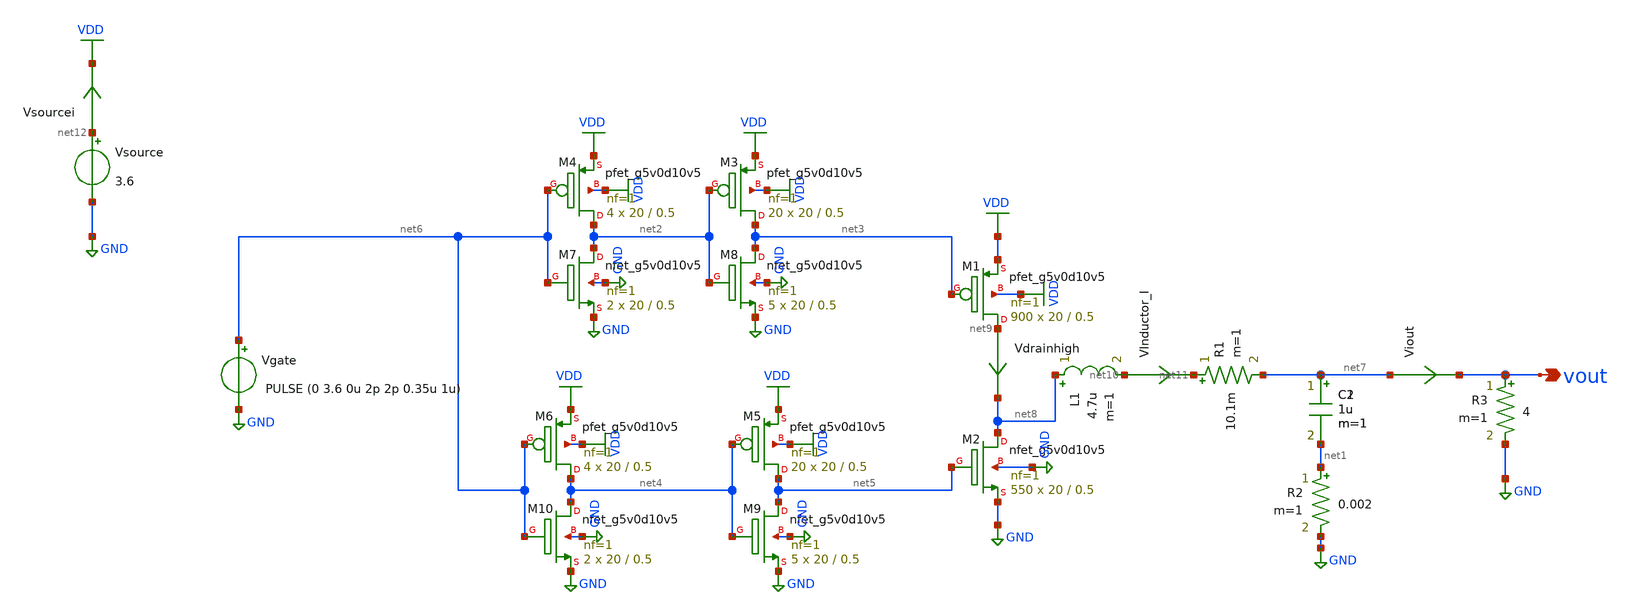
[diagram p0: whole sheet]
** sch_path: SMPS_Without_Deadtime/buck_converter.sch
**.subckt buck_converter vout
*.opin vout
XM1 net9 net3 VDD VDD sky130_fd_pr__pfet_g5v0d10v5 L=0.5 W=20 nf=1 ad='int((nf+1)/2) * W/nf * 0.29' as='int((nf+2)/2) * W/nf * 0.29'
+ pd='2*int((nf+1)/2) * (W/nf + 0.29)' ps='2*int((nf+2)/2) * (W/nf + 0.29)' nrd='0.29 / W' nrs='0.29 / W'
+ sa=0 sb=0 sd=0 mult=900 m=900
XM2 net8 net5 GND GND sky130_fd_pr__nfet_g5v0d10v5 L=0.5 W=20 nf=1 ad='int((nf+1)/2) * W/nf * 0.29' as='int((nf+2)/2) * W/nf * 0.29'
+ pd='2*int((nf+1)/2) * (W/nf + 0.29)' ps='2*int((nf+2)/2) * (W/nf + 0.29)' nrd='0.29 / W' nrs='0.29 / W'
+ sa=0 sb=0 sd=0 mult=550 m=550
L1 net8 net10 4.7u m=1
R1 net11 net7 10.1m m=1
C1 net7 net1 1u m=1
R2 net1 GND 0.002 m=1
Vgate net6 GND PULSE (0 3.6 0u 2p 2p 0.35u 1u)
Vsource net12 GND 3.6
XM3 net3 net2 VDD VDD sky130_fd_pr__pfet_g5v0d10v5 L=0.5 W=20 nf=1 ad='int((nf+1)/2) * W/nf * 0.29' as='int((nf+2)/2) * W/nf * 0.29'
+ pd='2*int((nf+1)/2) * (W/nf + 0.29)' ps='2*int((nf+2)/2) * (W/nf + 0.29)' nrd='0.29 / W' nrs='0.29 / W'
+ sa=0 sb=0 sd=0 mult=20 m=20
XM4 net2 net6 VDD VDD sky130_fd_pr__pfet_g5v0d10v5 L=0.5 W=20 nf=1 ad='int((nf+1)/2) * W/nf * 0.29' as='int((nf+2)/2) * W/nf * 0.29'
+ pd='2*int((nf+1)/2) * (W/nf + 0.29)' ps='2*int((nf+2)/2) * (W/nf + 0.29)' nrd='0.29 / W' nrs='0.29 / W'
+ sa=0 sb=0 sd=0 mult=4 m=4
XM5 net5 net4 VDD VDD sky130_fd_pr__pfet_g5v0d10v5 L=0.5 W=20 nf=1 ad='int((nf+1)/2) * W/nf * 0.29' as='int((nf+2)/2) * W/nf * 0.29'
+ pd='2*int((nf+1)/2) * (W/nf + 0.29)' ps='2*int((nf+2)/2) * (W/nf + 0.29)' nrd='0.29 / W' nrs='0.29 / W'
+ sa=0 sb=0 sd=0 mult=20 m=20
XM6 net4 net6 VDD VDD sky130_fd_pr__pfet_g5v0d10v5 L=0.5 W=20 nf=1 ad='int((nf+1)/2) * W/nf * 0.29' as='int((nf+2)/2) * W/nf * 0.29'
+ pd='2*int((nf+1)/2) * (W/nf + 0.29)' ps='2*int((nf+2)/2) * (W/nf + 0.29)' nrd='0.29 / W' nrs='0.29 / W'
+ sa=0 sb=0 sd=0 mult=4 m=4
XM7 net2 net6 GND GND sky130_fd_pr__nfet_g5v0d10v5 L=0.5 W=20 nf=1 ad='int((nf+1)/2) * W/nf * 0.29' as='int((nf+2)/2) * W/nf * 0.29'
+ pd='2*int((nf+1)/2) * (W/nf + 0.29)' ps='2*int((nf+2)/2) * (W/nf + 0.29)' nrd='0.29 / W' nrs='0.29 / W'
+ sa=0 sb=0 sd=0 mult=2 m=2
XM8 net3 net2 GND GND sky130_fd_pr__nfet_g5v0d10v5 L=0.5 W=20 nf=1 ad='int((nf+1)/2) * W/nf * 0.29' as='int((nf+2)/2) * W/nf * 0.29'
+ pd='2*int((nf+1)/2) * (W/nf + 0.29)' ps='2*int((nf+2)/2) * (W/nf + 0.29)' nrd='0.29 / W' nrs='0.29 / W'
+ sa=0 sb=0 sd=0 mult=5 m=5
XM9 net5 net4 GND GND sky130_fd_pr__nfet_g5v0d10v5 L=0.5 W=20 nf=1 ad='int((nf+1)/2) * W/nf * 0.29' as='int((nf+2)/2) * W/nf * 0.29'
+ pd='2*int((nf+1)/2) * (W/nf + 0.29)' ps='2*int((nf+2)/2) * (W/nf + 0.29)' nrd='0.29 / W' nrs='0.29 / W'
+ sa=0 sb=0 sd=0 mult=5 m=5
XM10 net4 net6 GND GND sky130_fd_pr__nfet_g5v0d10v5 L=0.5 W=20 nf=1 ad='int((nf+1)/2) * W/nf * 0.29'
+ as='int((nf+2)/2) * W/nf * 0.29' pd='2*int((nf+1)/2) * (W/nf + 0.29)' ps='2*int((nf+2)/2) * (W/nf + 0.29)'
+ nrd='0.29 / W' nrs='0.29 / W' sa=0 sb=0 sd=0 mult=2 m=2
Vdrainhigh net9 net8 0
.save i(vdrainhigh)
Viout net7 vout 0
.save i(viout)
Vsourcei net12 VDD 0
.save i(vsourcei)
VInductor_I net10 net11 0
.save i(vinductor_i)
R3 vout GND 4 m=1
C2 net7 net1 1u m=1
**** begin user architecture code
  .lib $::SKYWATER_MODELS/sky130.lib.spice tt

.tran 1u 200u
.save all


.control
run
meas tran idd_avg INTEG i(Vsourcei) from=110u to=111u
meas tran iout_avg INTEG i(Viout) from=110u to=111u
meas tran vout_avg INTEG v(vout) from=110u to=111u
meas tran vout_max MAX v(vout) from=110u to=111u
meas tran vdd_avg INTEG v(vdd) from=110u to=111u
let idd_avg = idd_avg*1Meg
let iout_avg = iout_avg*1Meg
let vdd_avg = vdd_avg*1Meg
let vout_avg = vout_avg*1Meg
let power_in = (idd_avg)*vdd_avg
let power_out = (iout_avg)*vout_avg
let efficiency = (power_out/power_in)*100
print power_in
print power_out
print efficiency
print vout_avg
print vout_max-vout_avg
.endc










**** end user architecture code
**.ends
.GLOBAL VDD
.GLOBAL GND
.end
